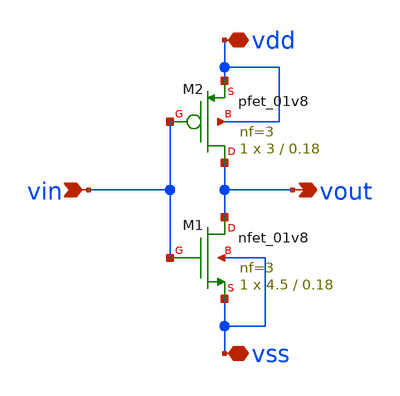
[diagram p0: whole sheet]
** sch_path: Lab1_inverter/xschem/inv.sch
**.subckt inv vin vout vdd vss
*.ipin vin
*.opin vout
*.iopin vdd
*.iopin vss
XM1 vout vin vss vss sky130_fd_pr__nfet_01v8 L=0.18 W=4.5 nf=3 ad='int((3 + 1)/2) * 4.5 / 3 * 0.29' as='int((3 + 2)/2) * 4.5 / 3 * 0.29'
+ pd='2*int((3 + 1)/2) * (4.5 / 3 + 0.29)' ps='2*int((3 + 2)/2) * (4.5 / 3 + 0.29)' nrd='0.29 / 4.5 ' nrs='0.29 / 4.5 '
+ sa=0 sb=0 sd=0 mult=1 m=1
XM2 vout vin vdd vdd sky130_fd_pr__pfet_01v8 L=0.18 W=3 nf=3 ad='int((3 + 1)/2) * 3 / 3 * 0.29' as='int((3 + 2)/2) * 3 / 3 * 0.29'
+ pd='2*int((3 + 1)/2) * (3 / 3 + 0.29)' ps='2*int((3 + 2)/2) * (3 / 3 + 0.29)' nrd='0.29 / 3 ' nrs='0.29 / 3 '
+ sa=0 sb=0 sd=0 mult=1 m=1
**.ends
.end
